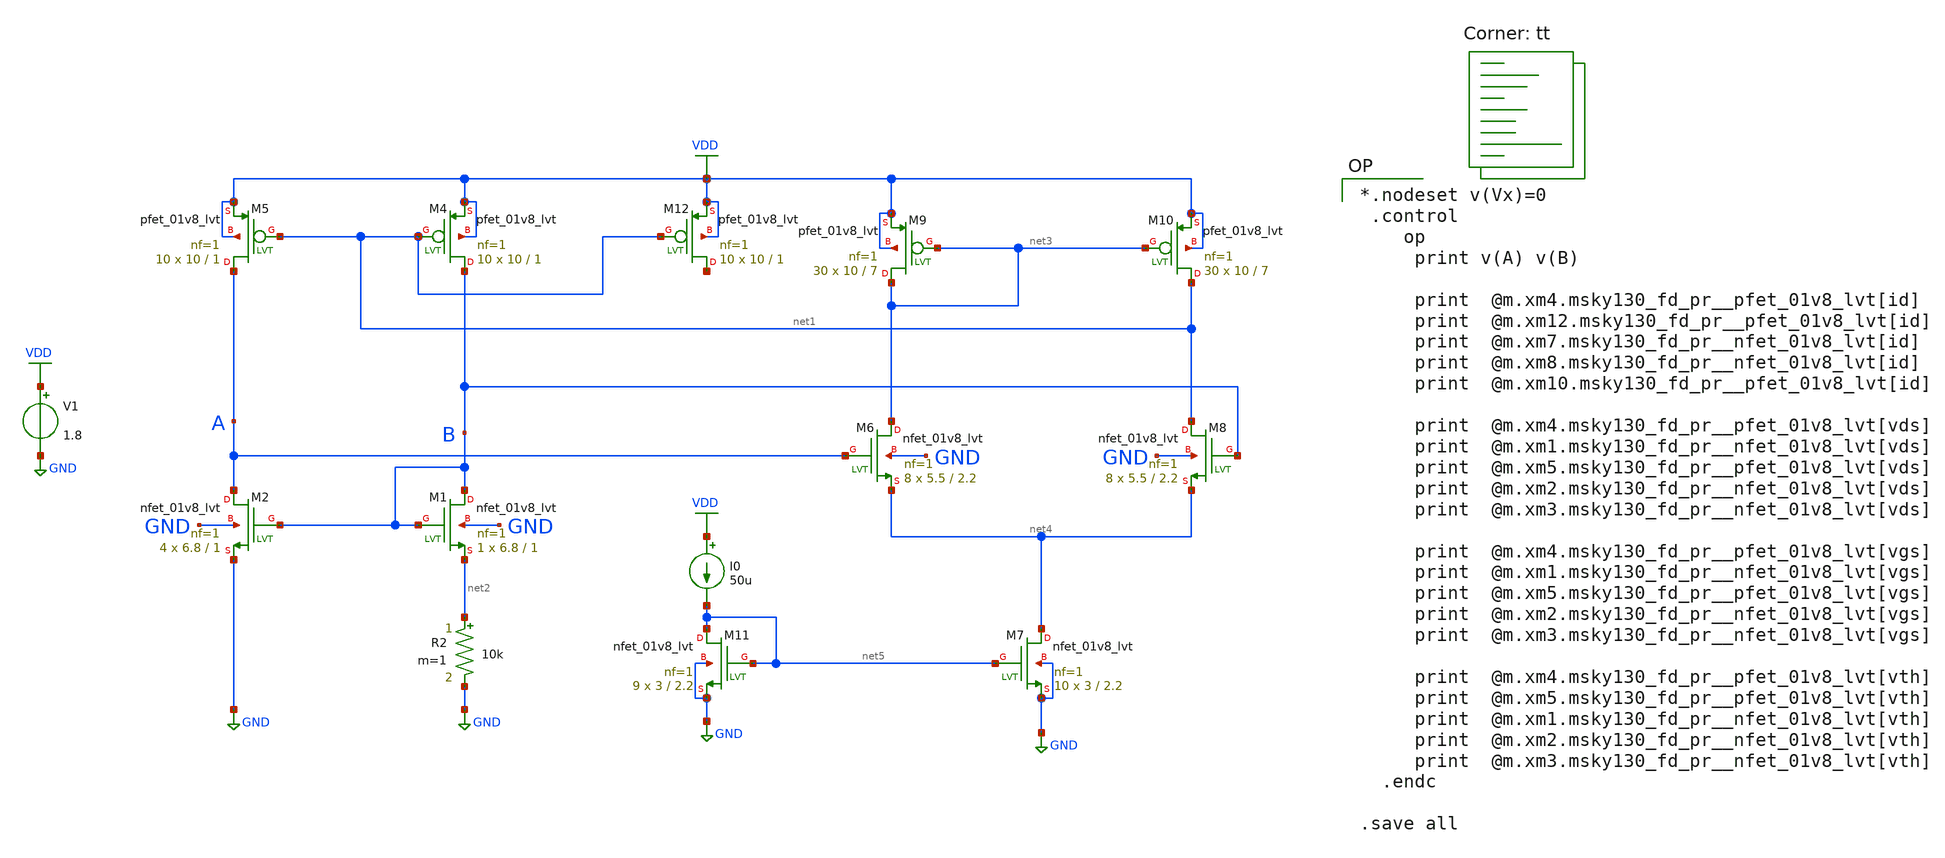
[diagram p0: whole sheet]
** sch_path: pll/lc_vco_lib/Hossam_Tarek/Biasing Circuits/xschem/constant GM1.sch
**.subckt constant GM1
XM1 B B net2 GND sky130_fd_pr__nfet_01v8_lvt L=1 W=6.8 nf=1 ad='int((nf+1)/2) * W/nf * 0.29' as='int((nf+2)/2) * W/nf * 0.29'
+ pd='2*int((nf+1)/2) * (W/nf + 0.29)' ps='2*int((nf+2)/2) * (W/nf + 0.29)' nrd='0.29 / W' nrs='0.29 / W'
+ sa=0 sb=0 sd=0 mult=1 m=1
XM2 A B GND GND sky130_fd_pr__nfet_01v8_lvt L=1 W=6.8 nf=1 ad='int((nf+1)/2) * W/nf * 0.29' as='int((nf+2)/2) * W/nf * 0.29'
+ pd='2*int((nf+1)/2) * (W/nf + 0.29)' ps='2*int((nf+2)/2) * (W/nf + 0.29)' nrd='0.29 / W' nrs='0.29 / W'
+ sa=0 sb=0 sd=0 mult=4 m=4
XM4 B net1 VDD VDD sky130_fd_pr__pfet_01v8_lvt L=1 W=10 nf=1 ad='int((nf+1)/2) * W/nf * 0.29' as='int((nf+2)/2) * W/nf * 0.29'
+ pd='2*int((nf+1)/2) * (W/nf + 0.29)' ps='2*int((nf+2)/2) * (W/nf + 0.29)' nrd='0.29 / W' nrs='0.29 / W'
+ sa=0 sb=0 sd=0 mult=10 m=10
XM5 A net1 VDD VDD sky130_fd_pr__pfet_01v8_lvt L=1 W=10 nf=1 ad='int((nf+1)/2) * W/nf * 0.29' as='int((nf+2)/2) * W/nf * 0.29'
+ pd='2*int((nf+1)/2) * (W/nf + 0.29)' ps='2*int((nf+2)/2) * (W/nf + 0.29)' nrd='0.29 / W' nrs='0.29 / W'
+ sa=0 sb=0 sd=0 mult=10 m=10
V1 VDD GND 1.8
R2 net2 GND 10k m=1
XM6 net3 A net4 GND sky130_fd_pr__nfet_01v8_lvt L=2.2 W=5.5 nf=1 ad='int((nf+1)/2) * W/nf * 0.29' as='int((nf+2)/2) * W/nf * 0.29'
+ pd='2*int((nf+1)/2) * (W/nf + 0.29)' ps='2*int((nf+2)/2) * (W/nf + 0.29)' nrd='0.29 / W' nrs='0.29 / W'
+ sa=0 sb=0 sd=0 mult=8 m=8
XM7 net4 net5 GND GND sky130_fd_pr__nfet_01v8_lvt L=2.2 W=3 nf=1 ad='int((nf+1)/2) * W/nf * 0.29' as='int((nf+2)/2) * W/nf * 0.29'
+ pd='2*int((nf+1)/2) * (W/nf + 0.29)' ps='2*int((nf+2)/2) * (W/nf + 0.29)' nrd='0.29 / W' nrs='0.29 / W'
+ sa=0 sb=0 sd=0 mult=10 m=10
XM8 net1 B net4 GND sky130_fd_pr__nfet_01v8_lvt L=2.2 W=5.5 nf=1 ad='int((nf+1)/2) * W/nf * 0.29' as='int((nf+2)/2) * W/nf * 0.29'
+ pd='2*int((nf+1)/2) * (W/nf + 0.29)' ps='2*int((nf+2)/2) * (W/nf + 0.29)' nrd='0.29 / W' nrs='0.29 / W'
+ sa=0 sb=0 sd=0 mult=8 m=8
XM9 net3 net3 VDD VDD sky130_fd_pr__pfet_01v8_lvt L=7 W=10 nf=1 ad='int((nf+1)/2) * W/nf * 0.29' as='int((nf+2)/2) * W/nf * 0.29'
+ pd='2*int((nf+1)/2) * (W/nf + 0.29)' ps='2*int((nf+2)/2) * (W/nf + 0.29)' nrd='0.29 / W' nrs='0.29 / W'
+ sa=0 sb=0 sd=0 mult=30 m=30
XM10 net1 net3 VDD VDD sky130_fd_pr__pfet_01v8_lvt L=7 W=10 nf=1 ad='int((nf+1)/2) * W/nf * 0.29' as='int((nf+2)/2) * W/nf * 0.29'
+ pd='2*int((nf+1)/2) * (W/nf + 0.29)' ps='2*int((nf+2)/2) * (W/nf + 0.29)' nrd='0.29 / W' nrs='0.29 / W'
+ sa=0 sb=0 sd=0 mult=30 m=30
XM11 net5 net5 GND GND sky130_fd_pr__nfet_01v8_lvt L=2.2 W=3 nf=1 ad='int((nf+1)/2) * W/nf * 0.29' as='int((nf+2)/2) * W/nf * 0.29'
+ pd='2*int((nf+1)/2) * (W/nf + 0.29)' ps='2*int((nf+2)/2) * (W/nf + 0.29)' nrd='0.29 / W' nrs='0.29 / W'
+ sa=0 sb=0 sd=0 mult=9 m=9
XM12 net6 net1 VDD VDD sky130_fd_pr__pfet_01v8_lvt L=1 W=10 nf=1 ad='int((nf+1)/2) * W/nf * 0.29' as='int((nf+2)/2) * W/nf * 0.29'
+ pd='2*int((nf+1)/2) * (W/nf + 0.29)' ps='2*int((nf+2)/2) * (W/nf + 0.29)' nrd='0.29 / W' nrs='0.29 / W'
+ sa=0 sb=0 sd=0 mult=10 m=10
I0 VDD net5 50u
**** begin user architecture code

*.nodeset v(Vx)=0
 .control
    op
     print v(A) v(B)

     print  @m.xm4.msky130_fd_pr__pfet_01v8_lvt[id]
     print  @m.xm12.msky130_fd_pr__pfet_01v8_lvt[id]
     print  @m.xm7.msky130_fd_pr__nfet_01v8_lvt[id]
     print  @m.xm8.msky130_fd_pr__nfet_01v8_lvt[id]
     print  @m.xm10.msky130_fd_pr__pfet_01v8_lvt[id]

     print  @m.xm4.msky130_fd_pr__pfet_01v8_lvt[vds]
     print  @m.xm1.msky130_fd_pr__nfet_01v8_lvt[vds]
     print  @m.xm5.msky130_fd_pr__pfet_01v8_lvt[vds]
     print  @m.xm2.msky130_fd_pr__nfet_01v8_lvt[vds]
     print  @m.xm3.msky130_fd_pr__nfet_01v8_lvt[vds]

     print  @m.xm4.msky130_fd_pr__pfet_01v8_lvt[vgs]
     print  @m.xm1.msky130_fd_pr__nfet_01v8_lvt[vgs]
     print  @m.xm5.msky130_fd_pr__pfet_01v8_lvt[vgs]
     print  @m.xm2.msky130_fd_pr__nfet_01v8_lvt[vgs]
     print  @m.xm3.msky130_fd_pr__nfet_01v8_lvt[vgs]

     print  @m.xm4.msky130_fd_pr__pfet_01v8_lvt[vth]
     print  @m.xm5.msky130_fd_pr__pfet_01v8_lvt[vth]
     print  @m.xm1.msky130_fd_pr__nfet_01v8_lvt[vth]
     print  @m.xm2.msky130_fd_pr__nfet_01v8_lvt[vth]
     print  @m.xm3.msky130_fd_pr__nfet_01v8_lvt[vth]
  .endc

.save all

.lib $::SKYWATER_MODELS/sky130.lib.spice tt
**** end user architecture code
**.ends
.GLOBAL GND
.GLOBAL VDD
.end
